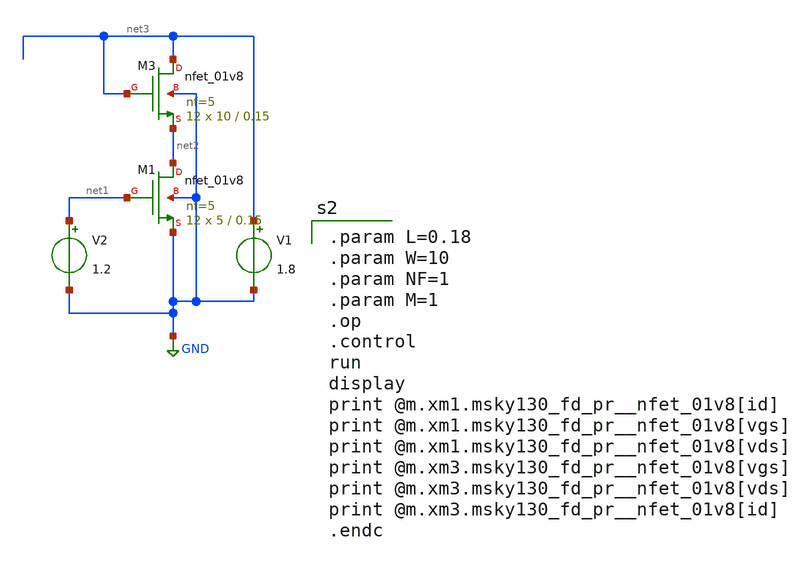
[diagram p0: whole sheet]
** sch_path: xschem/untitled-2.sch
**.subckt untitled-2
XM1 net2 net1 GND GND sky130_fd_pr__nfet_01v8 L=0.15 W=5 nf=5 ad='int((nf+1)/2) * W/nf * 0.29' as='int((nf+2)/2) * W/nf * 0.29'
+ pd='2*int((nf+1)/2) * (W/nf + 0.29)' ps='2*int((nf+2)/2) * (W/nf + 0.29)' nrd='0.29 / W' nrs='0.29 / W'
+ sa=0 sb=0 sd=0 mult=12 m=12
V1 net3 GND 1.8
XM3 net3 net3 net2 GND sky130_fd_pr__nfet_01v8 L=0.15 W=10 nf=5 ad='int((nf+1)/2) * W/nf * 0.29' as='int((nf+2)/2) * W/nf * 0.29'
+ pd='2*int((nf+1)/2) * (W/nf + 0.29)' ps='2*int((nf+2)/2) * (W/nf + 0.29)' nrd='0.29 / W' nrs='0.29 / W'
+ sa=0 sb=0 sd=0 mult=12 m=12
V2 net1 GND 1.2
**** begin user architecture code
.lib $::SKYWATER_MODELS/sky130.lib.spice tt
.include $::PDKPATH/libs.ref/sky130_fd_sc_hvl/spice/sky130_fd_sc_hvl.spice

.param L=0.18
.param W=10
.param NF=1
.param M=1
.op
.control
run
display
print @m.xm1.msky130_fd_pr__nfet_01v8[id]
print @m.xm1.msky130_fd_pr__nfet_01v8[vgs]
print @m.xm1.msky130_fd_pr__nfet_01v8[vds]
print @m.xm3.msky130_fd_pr__nfet_01v8[vgs]
print @m.xm3.msky130_fd_pr__nfet_01v8[vds]
print @m.xm3.msky130_fd_pr__nfet_01v8[id]
.endc


**** end user architecture code
**.ends
.GLOBAL GND
.end
